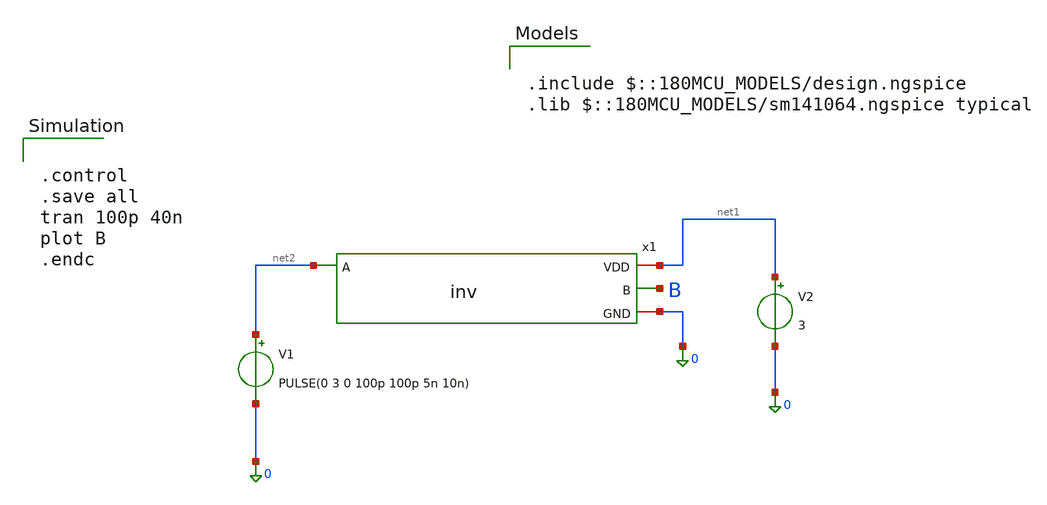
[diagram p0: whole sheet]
** sch_path: designs/libs/tb_analog/tb_inv/tb_inv.sch
**.subckt tb_inv
V1 net2 0 PULSE(0 3 0 100p 100p 5n 10n)
V2 net1 0 3
x1 net1 net2 B 0 inv
**** begin user architecture code


.control
.save all
tran 100p 40n
plot B
.endc



.include $::180MCU_MODELS/design.ngspice
.lib $::180MCU_MODELS/sm141064.ngspice typical

**** end user architecture code
**.ends

* expanding   symbol:  inv.sym # of pins=4
** sym_path: designs/libs/tb_analog/tb_inv/inv.sym
** sch_path: designs/libs/tb_analog/tb_inv/inv.sch
.subckt inv VDD A B GND
*.ipin A
*.opin B
*.iopin VDD
*.iopin GND
XM1 B A GND GND nfet_05v0 L=0.70u W=2u nf=1 ad='int((nf+1)/2) * W/nf * 0.18u' as='int((nf+2)/2) * W/nf * 0.18u'
+ pd='2*int((nf+1)/2) * (W/nf + 0.18u)' ps='2*int((nf+2)/2) * (W/nf + 0.18u)' nrd='0.18u / W' nrs='0.18u / W'
+ sa=0 sb=0 sd=0 m=1
XM2 B A VDD VDD pfet_05v0 L=0.7u W=5u nf=1 ad='int((nf+1)/2) * W/nf * 0.18u' as='int((nf+2)/2) * W/nf * 0.18u'
+ pd='2*int((nf+1)/2) * (W/nf + 0.18u)' ps='2*int((nf+2)/2) * (W/nf + 0.18u)' nrd='0.18u / W' nrs='0.18u / W'
+ sa=0 sb=0 sd=0 m=1
.ends

.end
